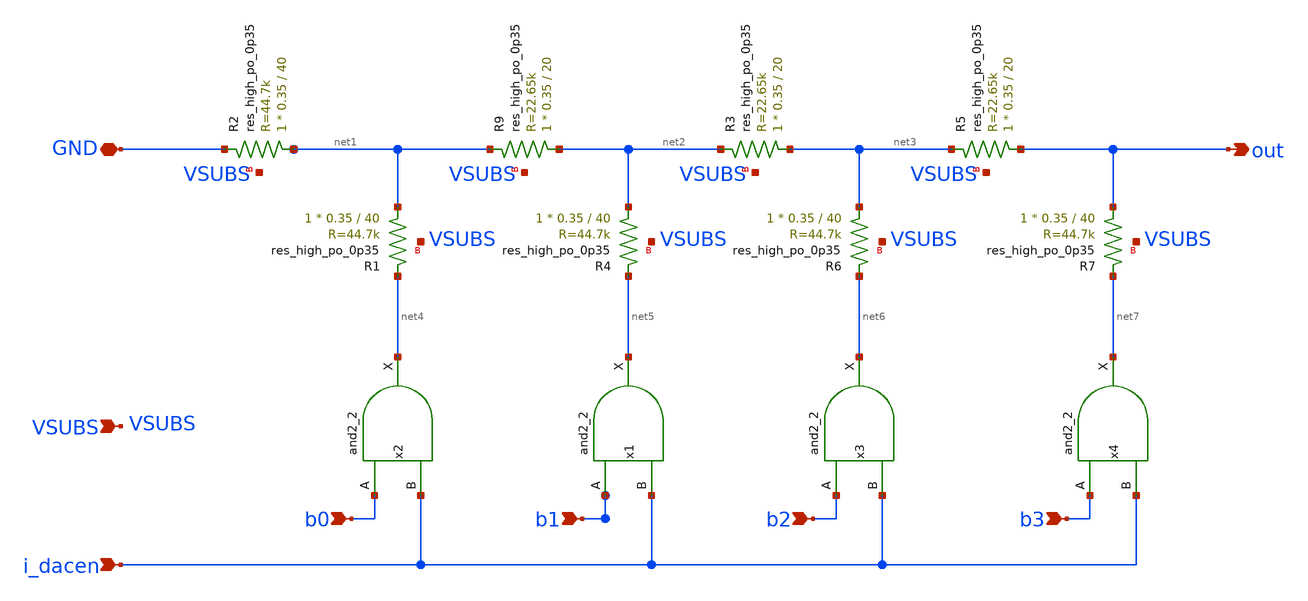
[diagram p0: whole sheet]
** sch_path: xschem/r2r_4b.sch
**.subckt r2r_4b GND out i_dacen b0 b2 b1 b3 VSUBS
*.iopin GND
*.opin out
*.ipin i_dacen
*.ipin b0
*.ipin b2
*.ipin b1
*.ipin b3
*.ipin VSUBS
XR2 net1 GND VSUBS sky130_fd_pr__res_high_po_0p35 L=40 mult=1 m=1
XR9 net2 net1 VSUBS sky130_fd_pr__res_high_po_0p35 L=20 mult=1 m=1
XR1 net1 net4 VSUBS sky130_fd_pr__res_high_po_0p35 L=40 mult=1 m=1
XR3 net3 net2 VSUBS sky130_fd_pr__res_high_po_0p35 L=20 mult=1 m=1
XR4 net2 net5 VSUBS sky130_fd_pr__res_high_po_0p35 L=40 mult=1 m=1
XR5 out net3 VSUBS sky130_fd_pr__res_high_po_0p35 L=20 mult=1 m=1
XR6 net3 net6 VSUBS sky130_fd_pr__res_high_po_0p35 L=40 mult=1 m=1
XR7 out net7 VSUBS sky130_fd_pr__res_high_po_0p35 L=40 mult=1 m=1
x2 b0 i_dacen VGND VNB VPB VPWR net4 sky130_fd_sc_hd__and2_2
x1 b1 i_dacen VGND VNB VPB VPWR net5 sky130_fd_sc_hd__and2_2
x3 b2 i_dacen VGND VNB VPB VPWR net6 sky130_fd_sc_hd__and2_2
x4 b3 i_dacen VGND VNB VPB VPWR net7 sky130_fd_sc_hd__and2_2
**.ends
.end
